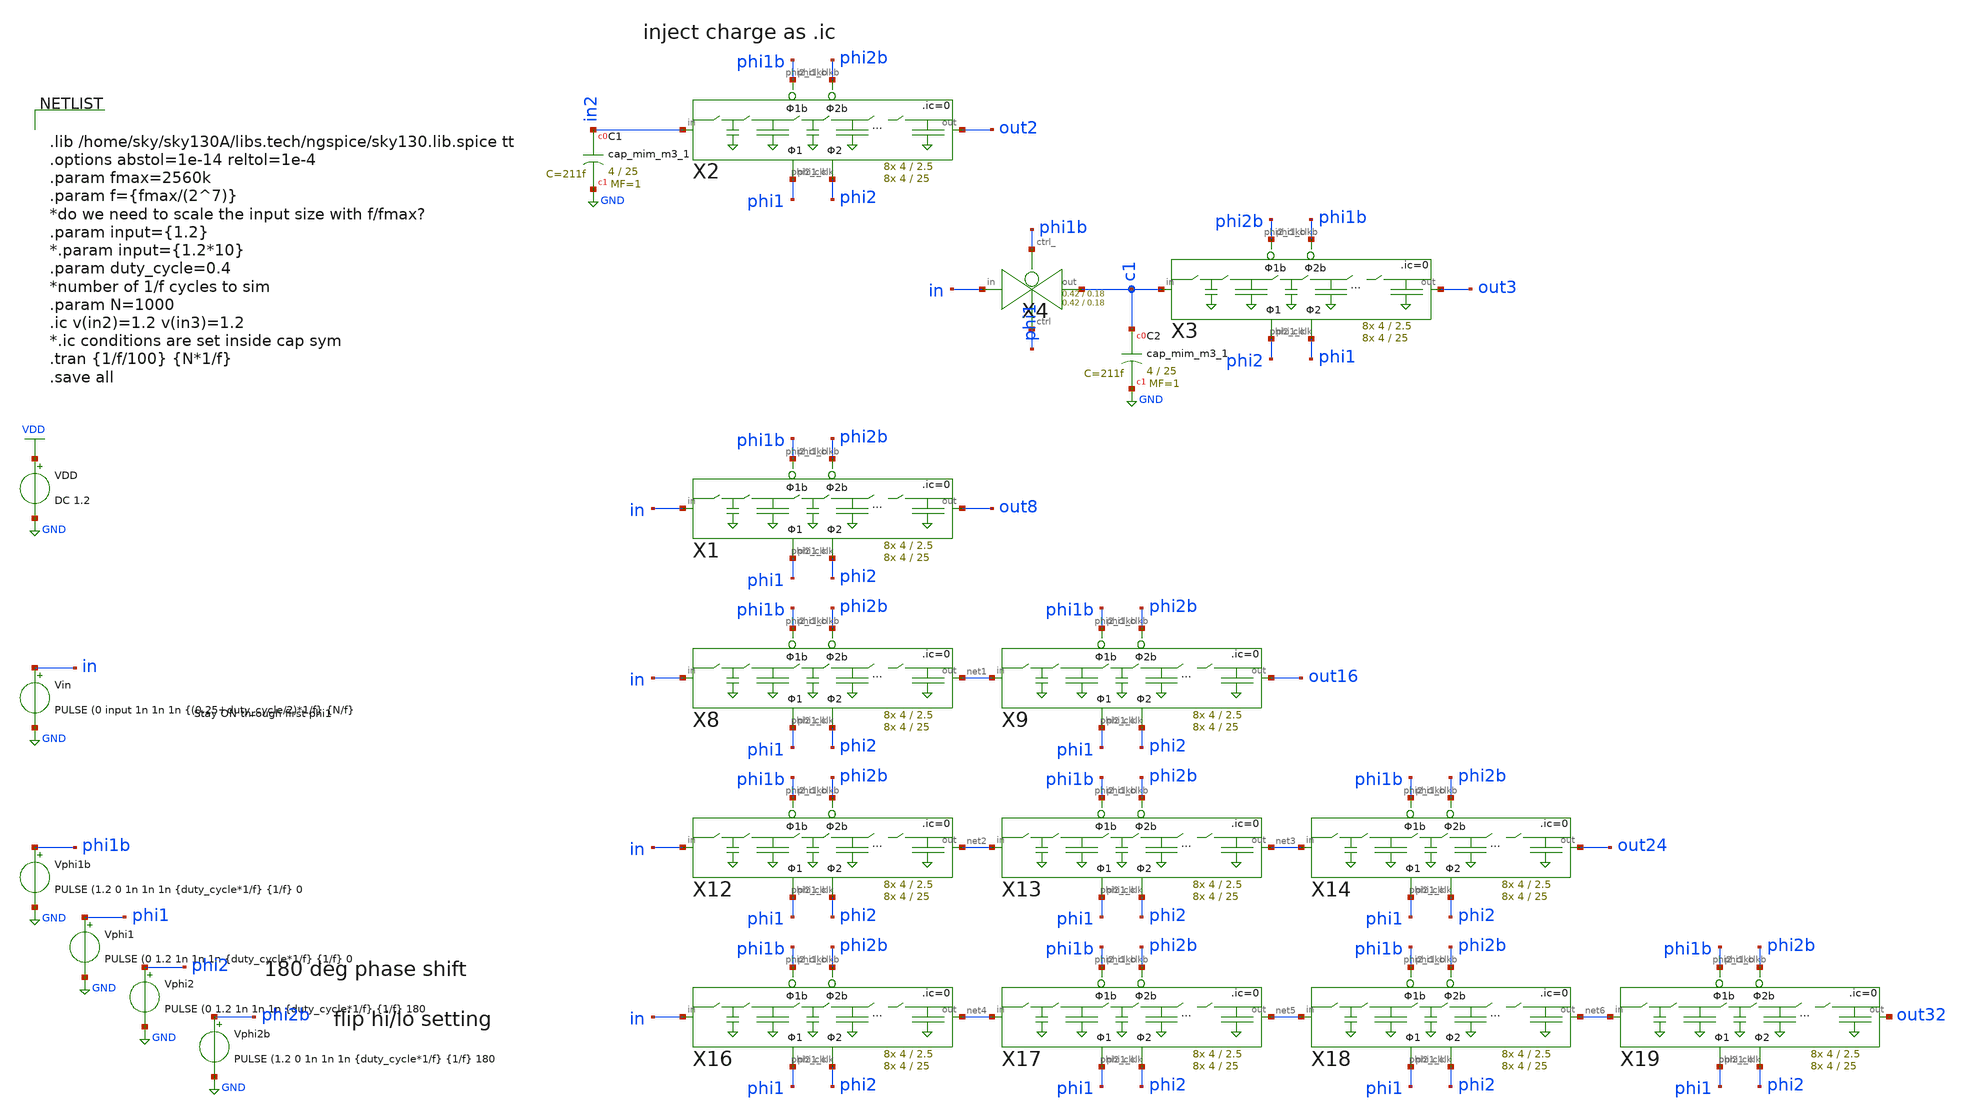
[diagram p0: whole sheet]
** sch_path: xschem/Switched_Caps/16switchcaps_2phi_tb.sch
**.subckt 16switchcaps_2phi_tb
Vin in GND PULSE (0 input 1n 1n 1n {(0.25+duty_cycle/2)*1/f} {N/f}
VDD VDD GND DC 1.2
Vphi1 phi1 GND PULSE (0 1.2 1n 1n 1n {duty_cycle*1/f} {1/f} 0
Vphi1b phi1b GND PULSE (1.2 0 1n 1n 1n {duty_cycle*1/f} {1/f} 0
Vphi2 phi2 GND PULSE (0 1.2 1n 1n 1n {duty_cycle*1/f} {1/f} 180
Vphi2b phi2b GND PULSE (1.2 0 1n 1n 1n {duty_cycle*1/f} {1/f} 180
X1 in out8 phi1 phi1b phi2 phi2b 16switchcaps_2phi Wcap1=4 Lcap1=2.5 Wcap2=4 Lcap2=25
X2 in2 out2 phi1 phi1b phi2 phi2b 16switchcaps_2phi Wcap1=4 Lcap1=2.5 Wcap2=4 Lcap2=25
XC1 in2 GND sky130_fd_pr__cap_mim_m3_1 W=4 L=25 MF=1 m=1
X3 c1 out3 phi2 phi2b phi1 phi1b 16switchcaps_2phi Wcap1=4 Lcap1=2.5 Wcap2=4 Lcap2=25
XC2 c1 GND sky130_fd_pr__cap_mim_m3_1 W=4 L=25 MF=1 m=1
X4 in c1 phi1b phi1 transmission_gate Wpmos=0.42 Lpmos=0.18 Wnmos=0.42 Lnmos=0.18
X8 in net1 phi1 phi1b phi2 phi2b 16switchcaps_2phi Wcap1=4 Lcap1=2.5 Wcap2=4 Lcap2=25
X9 net1 out16 phi1 phi1b phi2 phi2b 16switchcaps_2phi Wcap1=4 Lcap1=2.5 Wcap2=4 Lcap2=25
X12 in net2 phi1 phi1b phi2 phi2b 16switchcaps_2phi Wcap1=4 Lcap1=2.5 Wcap2=4 Lcap2=25
X13 net2 net3 phi1 phi1b phi2 phi2b 16switchcaps_2phi Wcap1=4 Lcap1=2.5 Wcap2=4 Lcap2=25
X14 net3 out24 phi1 phi1b phi2 phi2b 16switchcaps_2phi Wcap1=4 Lcap1=2.5 Wcap2=4 Lcap2=25
X16 in net4 phi1 phi1b phi2 phi2b 16switchcaps_2phi Wcap1=4 Lcap1=2.5 Wcap2=4 Lcap2=25
X17 net4 net5 phi1 phi1b phi2 phi2b 16switchcaps_2phi Wcap1=4 Lcap1=2.5 Wcap2=4 Lcap2=25
X18 net5 net6 phi1 phi1b phi2 phi2b 16switchcaps_2phi Wcap1=4 Lcap1=2.5 Wcap2=4 Lcap2=25
X19 net6 out32 phi1 phi1b phi2 phi2b 16switchcaps_2phi Wcap1=4 Lcap1=2.5 Wcap2=4 Lcap2=25
**** begin user architecture code


.lib /home/sky/sky130A/libs.tech/ngspice/sky130.lib.spice tt
.options abstol=1e-14 reltol=1e-4
.param fmax=2560k
.param f={fmax/(2^7)}
*do we need to scale the input size with f/fmax?
.param input={1.2}
*.param input={1.2*10}
.param duty_cycle=0.4
*number of 1/f cycles to sim
.param N=1000
.ic v(in2)=1.2 v(in3)=1.2
*.ic conditions are set inside cap sym
.tran {1/f/100} {N*1/f}
.save all


**** end user architecture code
**.ends
.GLOBAL GND
.GLOBAL VDD
.end
